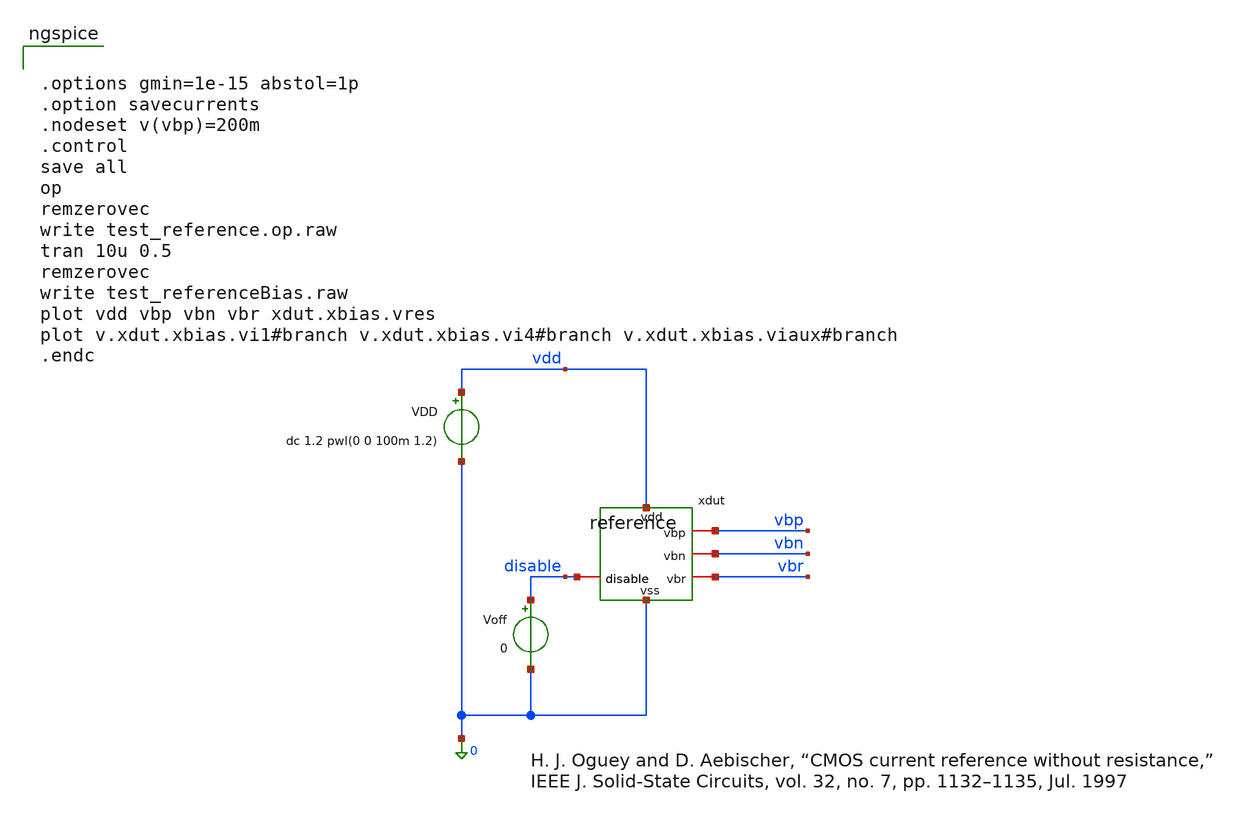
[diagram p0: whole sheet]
** sch_path: xschem/test_reference.sch
**.subckt test_reference
xdut vdd vbp vbn disable vbr 0 reference
VDD vdd 0 dc 1.2 pwl(0 0 100m 1.2)
Voff disable 0 0
**** begin user architecture code


.options gmin=1e-15 abstol=1p
.option savecurrents
.nodeset v(vbp)=200m
.control
save all
op
remzerovec
write test_reference.op.raw
tran 10u 0.5
remzerovec
write test_referenceBias.raw
plot vdd vbp vbn vbr xdut.xbias.vres
plot v.xdut.xbias.vi1#branch v.xdut.xbias.vi4#branch v.xdut.xbias.viaux#branch
.endc


 .lib cornerMOShv.lib mos_tt

.param mc_mm_switch=0
.param mc_pr_switch=1


**** end user architecture code
**.ends
.end
